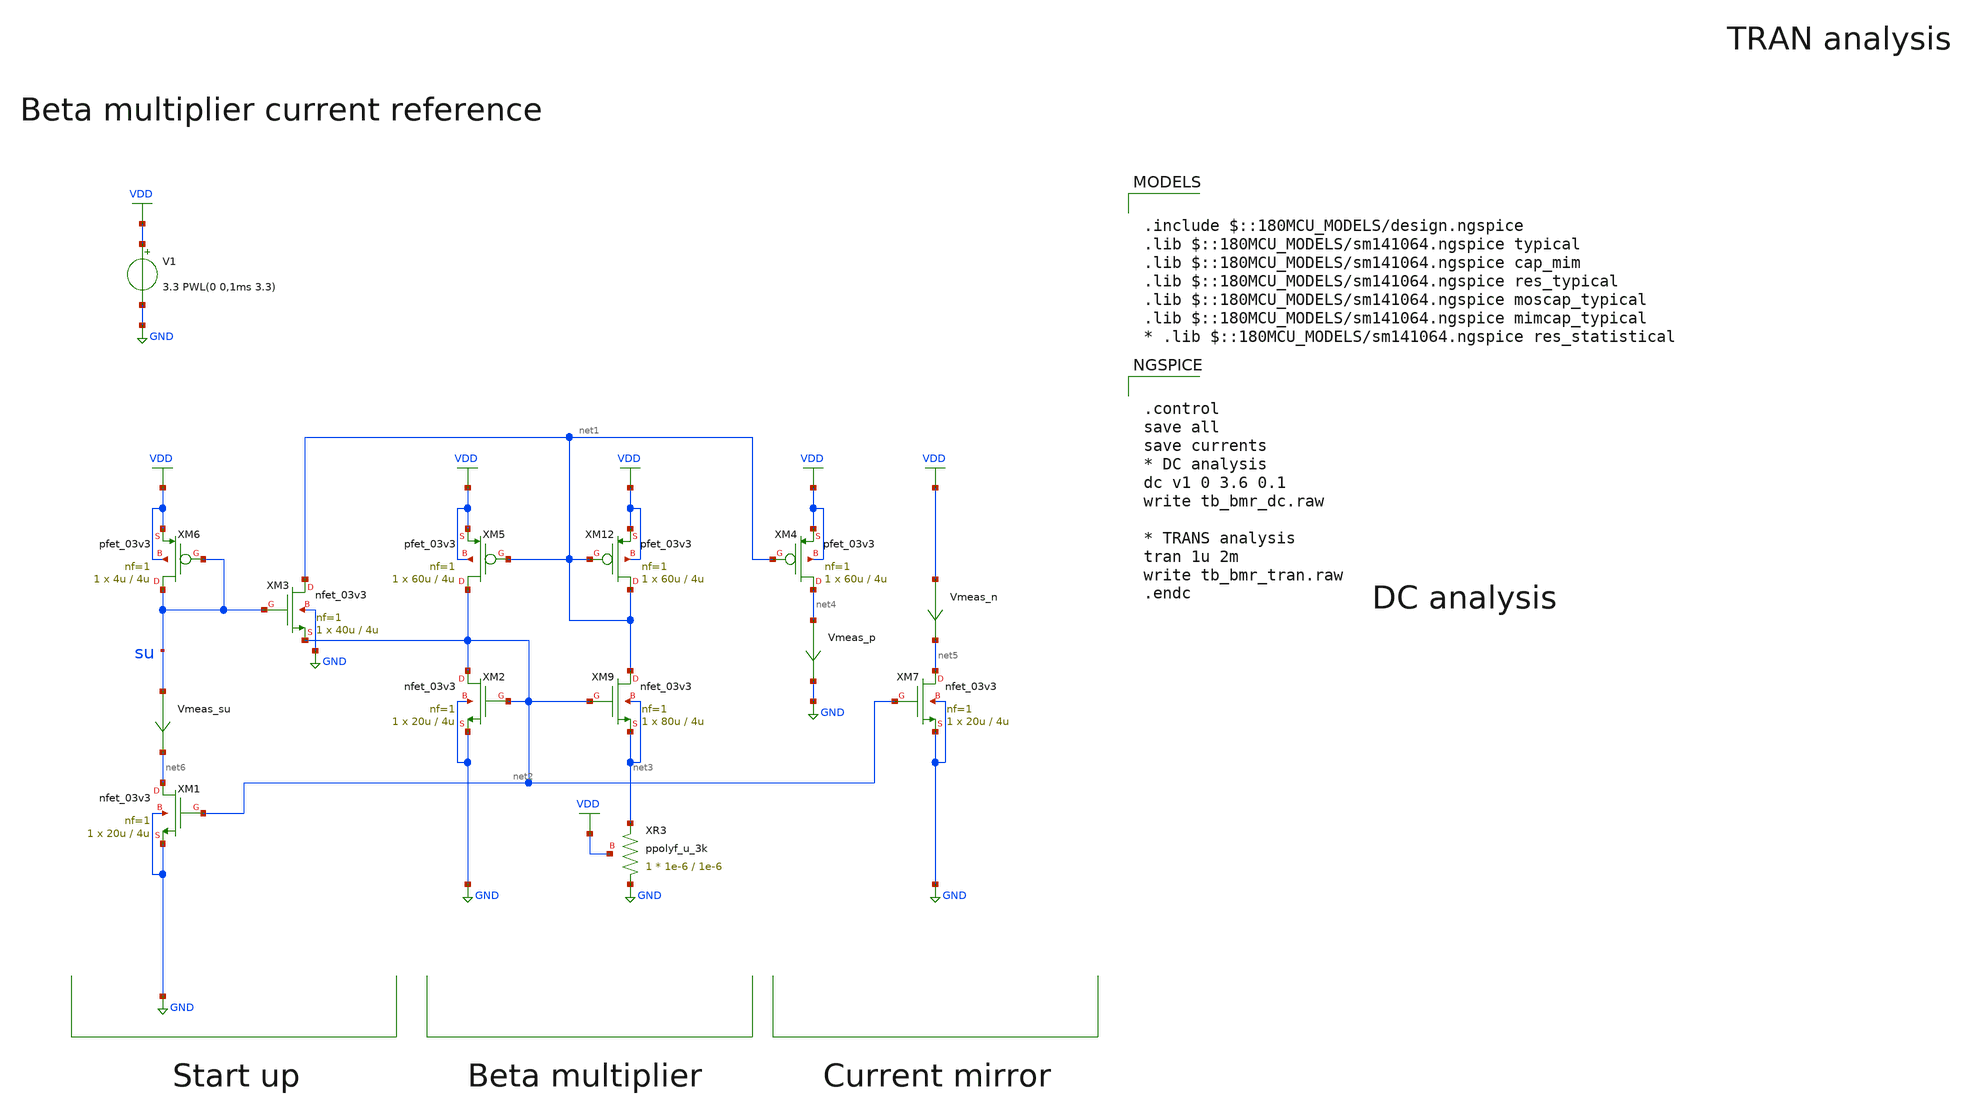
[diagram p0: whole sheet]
** sch_path: designs/libs/tb_analog/tb_bmr/tb_bmr.sch
* Copyright 2022 GlobalFoundries PDK Authors
* Licensed under the Apache License, Version 2.0 (the "License");
* you may not use this file except in compliance with the License.
* You may obtain a copy of the License at
* https://www.apache.org/licenses/LICENSE-2.0
* Unless required by applicable law or agreed to in writing, software
* distributed under the License is distributed on an "AS IS" BASIS,
* WITHOUT WARRANTIES OR CONDITIONS OF ANY KIND, either express or implied.
* See the License for the specific language governing permissions and
* limitations under the License.
**.subckt tb_bmr
V1 VDD GND 3.3 PWL(0 0,1ms 3.3)
XM3 net1 su net2 GND nfet_03v3 L=4u W=40u nf=1 ad='int((nf+1)/2) * W/nf * 0.18u' as='int((nf+2)/2) * W/nf * 0.18u'
+ pd='2*int((nf+1)/2) * (W/nf + 0.18u)' ps='2*int((nf+2)/2) * (W/nf + 0.18u)' nrd='0.18u / W' nrs='0.18u / W'
+ sa=0 sb=0 sd=0 m=1
XM5 net2 net1 VDD VDD pfet_03v3 L=4u W=60u nf=1 ad='int((nf+1)/2) * W/nf * 0.18u' as='int((nf+2)/2) * W/nf * 0.18u'
+ pd='2*int((nf+1)/2) * (W/nf + 0.18u)' ps='2*int((nf+2)/2) * (W/nf + 0.18u)' nrd='0.18u / W' nrs='0.18u / W'
+ sa=0 sb=0 sd=0 m=1
XM6 su su VDD VDD pfet_03v3 L=4u W=4u nf=1 ad='int((nf+1)/2) * W/nf * 0.18u' as='int((nf+2)/2) * W/nf * 0.18u'
+ pd='2*int((nf+1)/2) * (W/nf + 0.18u)' ps='2*int((nf+2)/2) * (W/nf + 0.18u)' nrd='0.18u / W' nrs='0.18u / W'
+ sa=0 sb=0 sd=0 m=1
XM9 net1 net2 net3 net3 nfet_03v3 L=4u W=80u nf=1 ad='int((nf+1)/2) * W/nf * 0.18u' as='int((nf+2)/2) * W/nf * 0.18u'
+ pd='2*int((nf+1)/2) * (W/nf + 0.18u)' ps='2*int((nf+2)/2) * (W/nf + 0.18u)' nrd='0.18u / W' nrs='0.18u / W'
+ sa=0 sb=0 sd=0 m=1
XM12 net1 net1 VDD VDD pfet_03v3 L=4u W=60u nf=1 ad='int((nf+1)/2) * W/nf * 0.18u' as='int((nf+2)/2) * W/nf * 0.18u'
+ pd='2*int((nf+1)/2) * (W/nf + 0.18u)' ps='2*int((nf+2)/2) * (W/nf + 0.18u)' nrd='0.18u / W' nrs='0.18u / W'
+ sa=0 sb=0 sd=0 m=1
XM1 net6 net2 GND GND nfet_03v3 L=4u W=20u nf=1 ad='int((nf+1)/2) * W/nf * 0.18u' as='int((nf+2)/2) * W/nf * 0.18u'
+ pd='2*int((nf+1)/2) * (W/nf + 0.18u)' ps='2*int((nf+2)/2) * (W/nf + 0.18u)' nrd='0.18u / W' nrs='0.18u / W'
+ sa=0 sb=0 sd=0 m=1
XM2 net2 net2 GND GND nfet_03v3 L=4u W=20u nf=1 ad='int((nf+1)/2) * W/nf * 0.18u' as='int((nf+2)/2) * W/nf * 0.18u'
+ pd='2*int((nf+1)/2) * (W/nf + 0.18u)' ps='2*int((nf+2)/2) * (W/nf + 0.18u)' nrd='0.18u / W' nrs='0.18u / W'
+ sa=0 sb=0 sd=0 m=1
XM4 net4 net1 VDD VDD pfet_03v3 L=4u W=60u nf=1 ad='int((nf+1)/2) * W/nf * 0.18u' as='int((nf+2)/2) * W/nf * 0.18u'
+ pd='2*int((nf+1)/2) * (W/nf + 0.18u)' ps='2*int((nf+2)/2) * (W/nf + 0.18u)' nrd='0.18u / W' nrs='0.18u / W'
+ sa=0 sb=0 sd=0 m=1
Vmeas_p net4 GND 0
.save i(vmeas_p)
XM7 net5 net2 GND GND nfet_03v3 L=4u W=20u nf=1 ad='int((nf+1)/2) * W/nf * 0.18u' as='int((nf+2)/2) * W/nf * 0.18u'
+ pd='2*int((nf+1)/2) * (W/nf + 0.18u)' ps='2*int((nf+2)/2) * (W/nf + 0.18u)' nrd='0.18u / W' nrs='0.18u / W'
+ sa=0 sb=0 sd=0 m=1
Vmeas_n VDD net5 0
.save i(vmeas_n)
XR3 GND net3 VDD ppolyf_u_3k r_width=1e-6 r_length=1e-6 m=1
Vmeas_su su net6 0
.save i(vmeas_su)
**** begin user architecture code


.control
save all
save currents
* DC analysis
dc v1 0 3.6 0.1
write tb_bmr_dc.raw

* TRANS analysis
tran 1u 2m
write tb_bmr_tran.raw
.endc



.include $::180MCU_MODELS/design.ngspice
.lib $::180MCU_MODELS/sm141064.ngspice typical
.lib $::180MCU_MODELS/sm141064.ngspice cap_mim
.lib $::180MCU_MODELS/sm141064.ngspice res_typical
.lib $::180MCU_MODELS/sm141064.ngspice moscap_typical
.lib $::180MCU_MODELS/sm141064.ngspice mimcap_typical
* .lib $::180MCU_MODELS/sm141064.ngspice res_statistical

**** end user architecture code
**.ends
.GLOBAL GND
.GLOBAL VDD
.end
